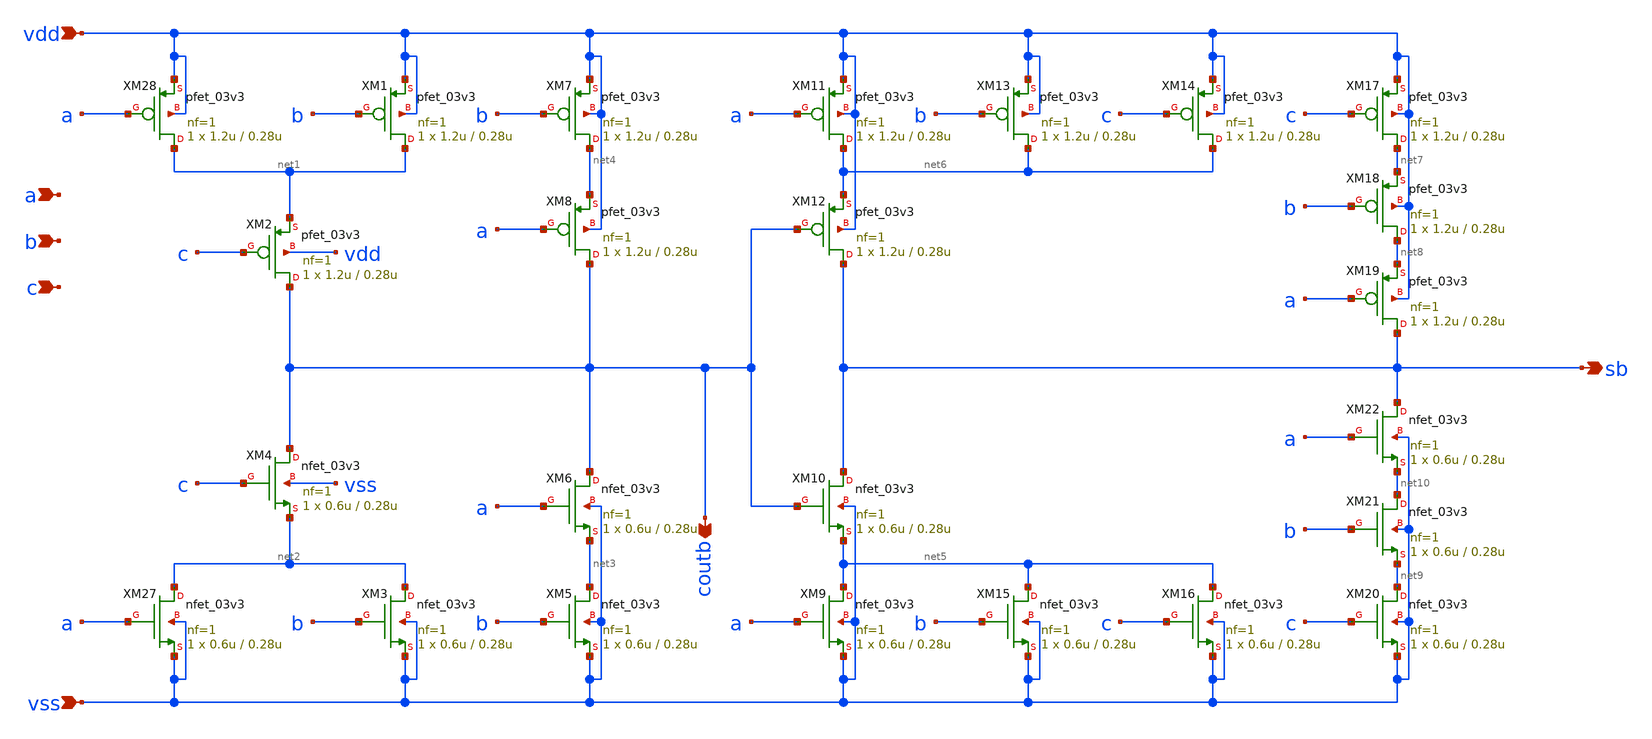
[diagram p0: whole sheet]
** sch_path: xschem/fulladder.sch
**.subckt fulladder sb coutb vss vdd a b c
*.opin sb
*.opin coutb
*.ipin vss
*.ipin vdd
*.ipin a
*.ipin b
*.ipin c
XM27 net2 a vss vss nfet_03v3 L=0.28u W=0.6u nf=1 ad='int((nf+1)/2) * W/nf * 0.18u' as='int((nf+2)/2) * W/nf * 0.18u'
+ pd='2*int((nf+1)/2) * (W/nf + 0.18u)' ps='2*int((nf+2)/2) * (W/nf + 0.18u)' nrd='0.18u / W' nrs='0.18u / W'
+ sa=0 sb=0 sd=0 m=1
XM28 net1 a vdd vdd pfet_03v3 L=0.28u W=1.2u nf=1 ad='int((nf+1)/2) * W/nf * 0.18u' as='int((nf+2)/2) * W/nf * 0.18u'
+ pd='2*int((nf+1)/2) * (W/nf + 0.18u)' ps='2*int((nf+2)/2) * (W/nf + 0.18u)' nrd='0.18u / W' nrs='0.18u / W'
+ sa=0 sb=0 sd=0 m=1
XM1 net1 b vdd vdd pfet_03v3 L=0.28u W=1.2u nf=1 ad='int((nf+1)/2) * W/nf * 0.18u' as='int((nf+2)/2) * W/nf * 0.18u'
+ pd='2*int((nf+1)/2) * (W/nf + 0.18u)' ps='2*int((nf+2)/2) * (W/nf + 0.18u)' nrd='0.18u / W' nrs='0.18u / W'
+ sa=0 sb=0 sd=0 m=1
XM2 coutb c net1 vdd pfet_03v3 L=0.28u W=1.2u nf=1 ad='int((nf+1)/2) * W/nf * 0.18u' as='int((nf+2)/2) * W/nf * 0.18u'
+ pd='2*int((nf+1)/2) * (W/nf + 0.18u)' ps='2*int((nf+2)/2) * (W/nf + 0.18u)' nrd='0.18u / W' nrs='0.18u / W'
+ sa=0 sb=0 sd=0 m=1
XM3 net2 b vss vss nfet_03v3 L=0.28u W=0.6u nf=1 ad='int((nf+1)/2) * W/nf * 0.18u' as='int((nf+2)/2) * W/nf * 0.18u'
+ pd='2*int((nf+1)/2) * (W/nf + 0.18u)' ps='2*int((nf+2)/2) * (W/nf + 0.18u)' nrd='0.18u / W' nrs='0.18u / W'
+ sa=0 sb=0 sd=0 m=1
XM4 coutb c net2 vss nfet_03v3 L=0.28u W=0.6u nf=1 ad='int((nf+1)/2) * W/nf * 0.18u' as='int((nf+2)/2) * W/nf * 0.18u'
+ pd='2*int((nf+1)/2) * (W/nf + 0.18u)' ps='2*int((nf+2)/2) * (W/nf + 0.18u)' nrd='0.18u / W' nrs='0.18u / W'
+ sa=0 sb=0 sd=0 m=1
XM5 net3 b vss vss nfet_03v3 L=0.28u W=0.6u nf=1 ad='int((nf+1)/2) * W/nf * 0.18u' as='int((nf+2)/2) * W/nf * 0.18u'
+ pd='2*int((nf+1)/2) * (W/nf + 0.18u)' ps='2*int((nf+2)/2) * (W/nf + 0.18u)' nrd='0.18u / W' nrs='0.18u / W'
+ sa=0 sb=0 sd=0 m=1
XM6 coutb a net3 vss nfet_03v3 L=0.28u W=0.6u nf=1 ad='int((nf+1)/2) * W/nf * 0.18u' as='int((nf+2)/2) * W/nf * 0.18u'
+ pd='2*int((nf+1)/2) * (W/nf + 0.18u)' ps='2*int((nf+2)/2) * (W/nf + 0.18u)' nrd='0.18u / W' nrs='0.18u / W'
+ sa=0 sb=0 sd=0 m=1
XM7 net4 b vdd vdd pfet_03v3 L=0.28u W=1.2u nf=1 ad='int((nf+1)/2) * W/nf * 0.18u' as='int((nf+2)/2) * W/nf * 0.18u'
+ pd='2*int((nf+1)/2) * (W/nf + 0.18u)' ps='2*int((nf+2)/2) * (W/nf + 0.18u)' nrd='0.18u / W' nrs='0.18u / W'
+ sa=0 sb=0 sd=0 m=1
XM8 coutb a net4 vdd pfet_03v3 L=0.28u W=1.2u nf=1 ad='int((nf+1)/2) * W/nf * 0.18u' as='int((nf+2)/2) * W/nf * 0.18u'
+ pd='2*int((nf+1)/2) * (W/nf + 0.18u)' ps='2*int((nf+2)/2) * (W/nf + 0.18u)' nrd='0.18u / W' nrs='0.18u / W'
+ sa=0 sb=0 sd=0 m=1
XM9 net5 a vss vss nfet_03v3 L=0.28u W=0.6u nf=1 ad='int((nf+1)/2) * W/nf * 0.18u' as='int((nf+2)/2) * W/nf * 0.18u'
+ pd='2*int((nf+1)/2) * (W/nf + 0.18u)' ps='2*int((nf+2)/2) * (W/nf + 0.18u)' nrd='0.18u / W' nrs='0.18u / W'
+ sa=0 sb=0 sd=0 m=1
XM10 sb coutb net5 vss nfet_03v3 L=0.28u W=0.6u nf=1 ad='int((nf+1)/2) * W/nf * 0.18u' as='int((nf+2)/2) * W/nf * 0.18u'
+ pd='2*int((nf+1)/2) * (W/nf + 0.18u)' ps='2*int((nf+2)/2) * (W/nf + 0.18u)' nrd='0.18u / W' nrs='0.18u / W'
+ sa=0 sb=0 sd=0 m=1
XM11 net6 a vdd vdd pfet_03v3 L=0.28u W=1.2u nf=1 ad='int((nf+1)/2) * W/nf * 0.18u' as='int((nf+2)/2) * W/nf * 0.18u'
+ pd='2*int((nf+1)/2) * (W/nf + 0.18u)' ps='2*int((nf+2)/2) * (W/nf + 0.18u)' nrd='0.18u / W' nrs='0.18u / W'
+ sa=0 sb=0 sd=0 m=1
XM12 sb coutb net6 vdd pfet_03v3 L=0.28u W=1.2u nf=1 ad='int((nf+1)/2) * W/nf * 0.18u' as='int((nf+2)/2) * W/nf * 0.18u'
+ pd='2*int((nf+1)/2) * (W/nf + 0.18u)' ps='2*int((nf+2)/2) * (W/nf + 0.18u)' nrd='0.18u / W' nrs='0.18u / W'
+ sa=0 sb=0 sd=0 m=1
XM13 net6 b vdd vdd pfet_03v3 L=0.28u W=1.2u nf=1 ad='int((nf+1)/2) * W/nf * 0.18u' as='int((nf+2)/2) * W/nf * 0.18u'
+ pd='2*int((nf+1)/2) * (W/nf + 0.18u)' ps='2*int((nf+2)/2) * (W/nf + 0.18u)' nrd='0.18u / W' nrs='0.18u / W'
+ sa=0 sb=0 sd=0 m=1
XM14 net6 c vdd vdd pfet_03v3 L=0.28u W=1.2u nf=1 ad='int((nf+1)/2) * W/nf * 0.18u' as='int((nf+2)/2) * W/nf * 0.18u'
+ pd='2*int((nf+1)/2) * (W/nf + 0.18u)' ps='2*int((nf+2)/2) * (W/nf + 0.18u)' nrd='0.18u / W' nrs='0.18u / W'
+ sa=0 sb=0 sd=0 m=1
XM15 net5 b vss vss nfet_03v3 L=0.28u W=0.6u nf=1 ad='int((nf+1)/2) * W/nf * 0.18u' as='int((nf+2)/2) * W/nf * 0.18u'
+ pd='2*int((nf+1)/2) * (W/nf + 0.18u)' ps='2*int((nf+2)/2) * (W/nf + 0.18u)' nrd='0.18u / W' nrs='0.18u / W'
+ sa=0 sb=0 sd=0 m=1
XM16 net5 c vss vss nfet_03v3 L=0.28u W=0.6u nf=1 ad='int((nf+1)/2) * W/nf * 0.18u' as='int((nf+2)/2) * W/nf * 0.18u'
+ pd='2*int((nf+1)/2) * (W/nf + 0.18u)' ps='2*int((nf+2)/2) * (W/nf + 0.18u)' nrd='0.18u / W' nrs='0.18u / W'
+ sa=0 sb=0 sd=0 m=1
XM17 net7 c vdd vdd pfet_03v3 L=0.28u W=1.2u nf=1 ad='int((nf+1)/2) * W/nf * 0.18u' as='int((nf+2)/2) * W/nf * 0.18u'
+ pd='2*int((nf+1)/2) * (W/nf + 0.18u)' ps='2*int((nf+2)/2) * (W/nf + 0.18u)' nrd='0.18u / W' nrs='0.18u / W'
+ sa=0 sb=0 sd=0 m=1
XM18 net8 b net7 vdd pfet_03v3 L=0.28u W=1.2u nf=1 ad='int((nf+1)/2) * W/nf * 0.18u' as='int((nf+2)/2) * W/nf * 0.18u'
+ pd='2*int((nf+1)/2) * (W/nf + 0.18u)' ps='2*int((nf+2)/2) * (W/nf + 0.18u)' nrd='0.18u / W' nrs='0.18u / W'
+ sa=0 sb=0 sd=0 m=1
XM19 sb a net8 vdd pfet_03v3 L=0.28u W=1.2u nf=1 ad='int((nf+1)/2) * W/nf * 0.18u' as='int((nf+2)/2) * W/nf * 0.18u'
+ pd='2*int((nf+1)/2) * (W/nf + 0.18u)' ps='2*int((nf+2)/2) * (W/nf + 0.18u)' nrd='0.18u / W' nrs='0.18u / W'
+ sa=0 sb=0 sd=0 m=1
XM20 net9 c vss vss nfet_03v3 L=0.28u W=0.6u nf=1 ad='int((nf+1)/2) * W/nf * 0.18u' as='int((nf+2)/2) * W/nf * 0.18u'
+ pd='2*int((nf+1)/2) * (W/nf + 0.18u)' ps='2*int((nf+2)/2) * (W/nf + 0.18u)' nrd='0.18u / W' nrs='0.18u / W'
+ sa=0 sb=0 sd=0 m=1
XM21 net10 b net9 vss nfet_03v3 L=0.28u W=0.6u nf=1 ad='int((nf+1)/2) * W/nf * 0.18u' as='int((nf+2)/2) * W/nf * 0.18u'
+ pd='2*int((nf+1)/2) * (W/nf + 0.18u)' ps='2*int((nf+2)/2) * (W/nf + 0.18u)' nrd='0.18u / W' nrs='0.18u / W'
+ sa=0 sb=0 sd=0 m=1
XM22 sb a net10 vss nfet_03v3 L=0.28u W=0.6u nf=1 ad='int((nf+1)/2) * W/nf * 0.18u' as='int((nf+2)/2) * W/nf * 0.18u'
+ pd='2*int((nf+1)/2) * (W/nf + 0.18u)' ps='2*int((nf+2)/2) * (W/nf + 0.18u)' nrd='0.18u / W' nrs='0.18u / W'
+ sa=0 sb=0 sd=0 m=1
**.ends
.end
